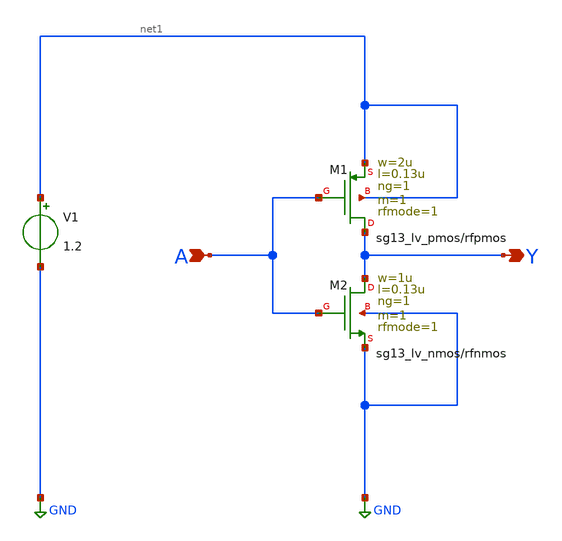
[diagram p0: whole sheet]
** sch_path: Team 1 Design/design_data/xschem/inverter/inverter.sch
**.subckt inverter A Y
*.ipin A
*.opin Y
XM1 Y A net1 net1 sg13_lv_pmos w=2u l=0.13u ng=1 m=1 rfmode=1 mm_ok=1
XM2 Y A GND GND sg13_lv_nmos w=1u l=0.13u ng=1 m=1 rfmode=1 mm_ok=1
V1 net1 GND 1.2
**.ends
.GLOBAL GND
.end
